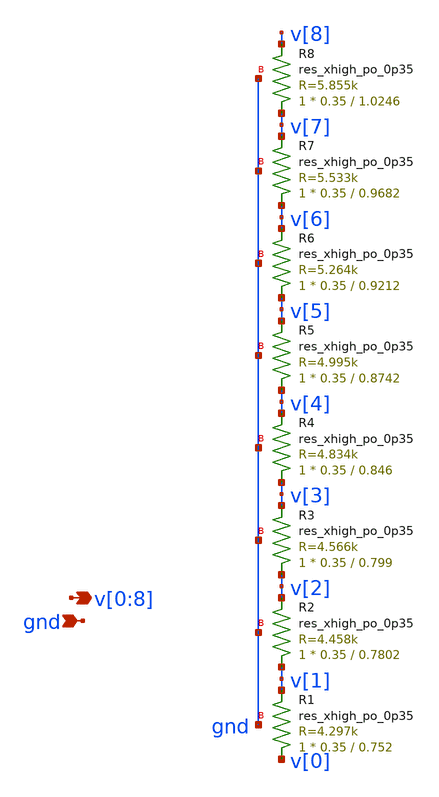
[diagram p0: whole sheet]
** sch_path: xschem/res_seg_3.sch
**.subckt res_seg_3 v[0],v[1],v[2],v[3],v[4],v[5],v[6],v[7],v[8] gnd
*.opin v[0],v[1],v[2],v[3],v[4],v[5],v[6],v[7],v[8]
*.ipin gnd
XR1 v[0] v[1] gnd sky130_fd_pr__res_xhigh_po_0p35 L=0.752 mult=1 m=1
XR2 v[1] v[2] gnd sky130_fd_pr__res_xhigh_po_0p35 L=0.7802 mult=1 m=1
XR3 v[2] v[3] gnd sky130_fd_pr__res_xhigh_po_0p35 L=0.799 mult=1 m=1
XR4 v[3] v[4] gnd sky130_fd_pr__res_xhigh_po_0p35 L=0.846 mult=1 m=1
XR5 v[4] v[5] gnd sky130_fd_pr__res_xhigh_po_0p35 L=0.8742 mult=1 m=1
XR6 v[5] v[6] gnd sky130_fd_pr__res_xhigh_po_0p35 L=0.9212 mult=1 m=1
XR7 v[6] v[7] gnd sky130_fd_pr__res_xhigh_po_0p35 L=0.9682 mult=1 m=1
XR8 v[7] v[8] gnd sky130_fd_pr__res_xhigh_po_0p35 L=1.0246 mult=1 m=1
**.ends
.end
